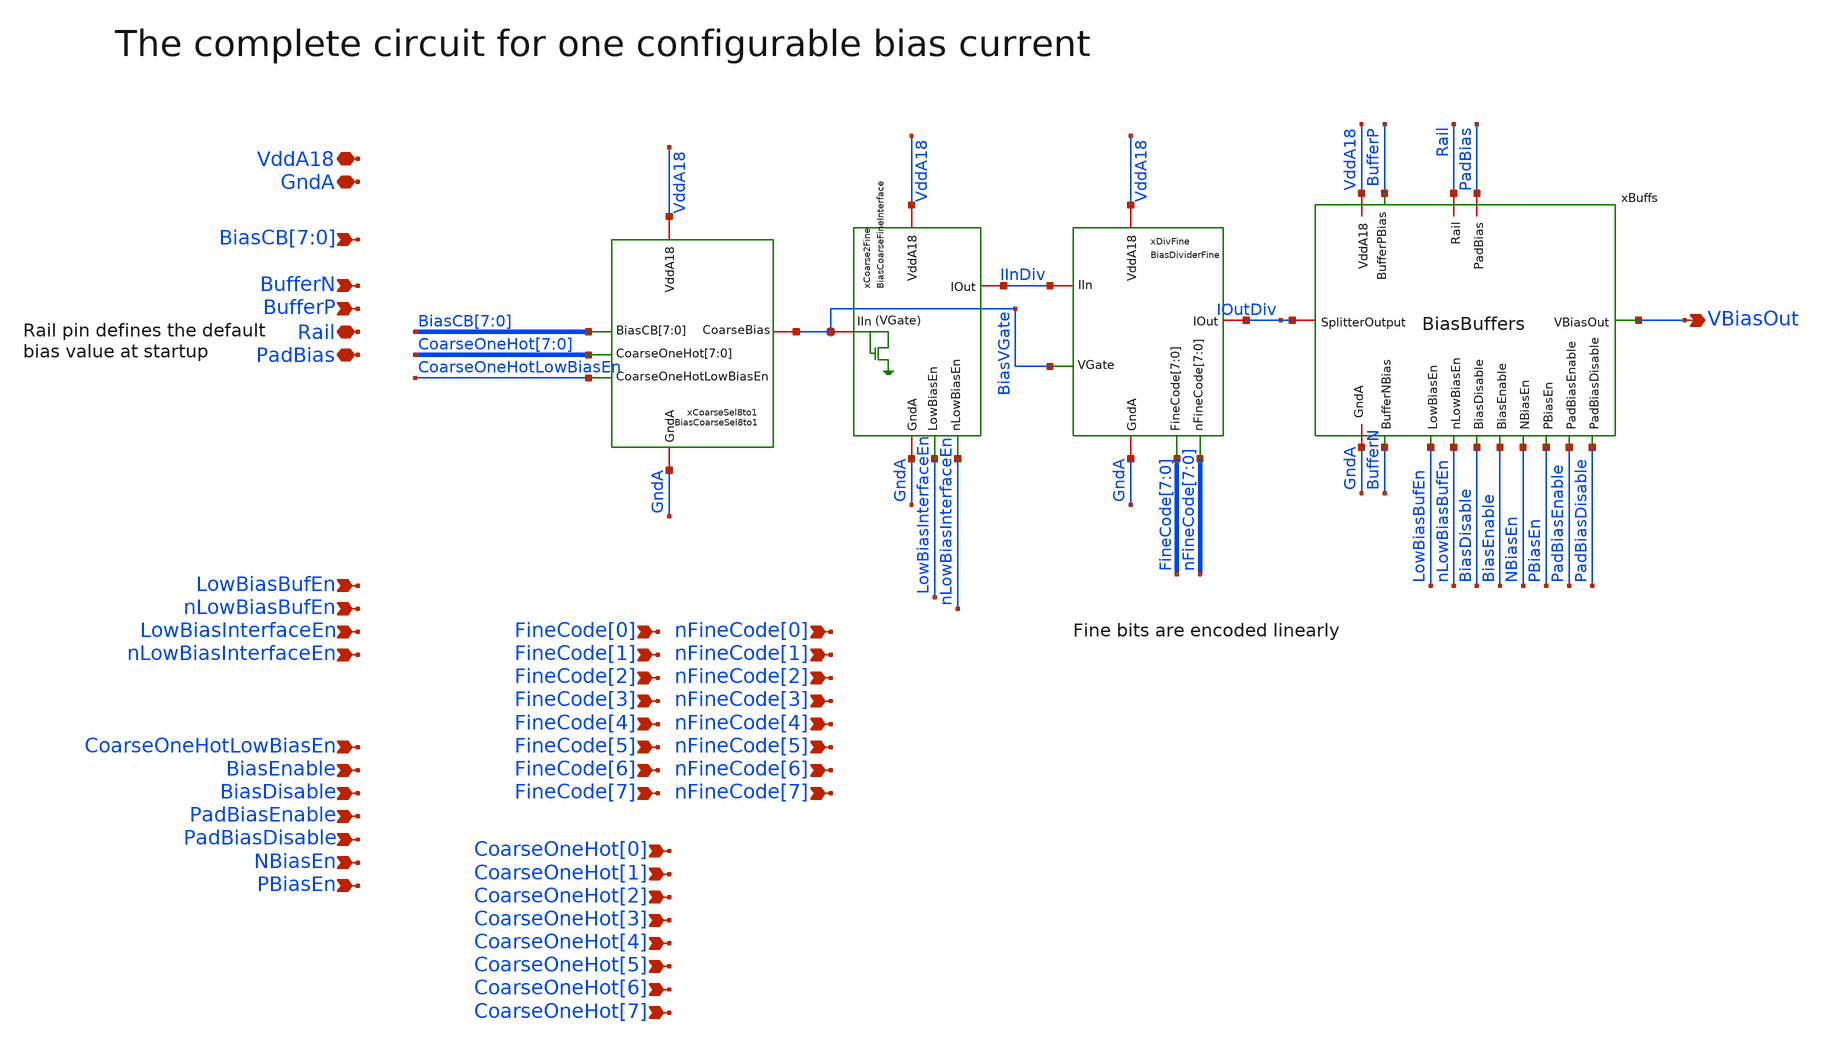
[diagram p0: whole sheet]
** sch_path: analog/xschem/BiasBranch.sch
**.subckt BiasBranch VddA18 GndA VBiasOut
*+ BiasCB[7],BiasCB[6],BiasCB[5],BiasCB[4],BiasCB[3],BiasCB[2],BiasCB[1],BiasCB[0] BufferN BufferP Rail LowBiasInterfaceEn nLowBiasInterfaceEn CoarseOneHotLowBiasEn LowBiasBufEn
*+ nLowBiasBufEn BiasEnable BiasDisable NBiasEn PBiasEn FineCode[0] FineCode[1] FineCode[2] FineCode[3] FineCode[4]
*+ FineCode[5] FineCode[6] FineCode[7] nFineCode[0] nFineCode[1] nFineCode[2] nFineCode[3] nFineCode[4]
*+ nFineCode[5] nFineCode[6] nFineCode[7] CoarseOneHot[0] CoarseOneHot[1] CoarseOneHot[2] CoarseOneHot[3]
*+ CoarseOneHot[4] CoarseOneHot[5] CoarseOneHot[6] CoarseOneHot[7] PadBiasEnable PadBiasDisable PadBias
*.iopin VddA18
*.iopin GndA
*.opin VBiasOut
*.ipin BiasCB[7],BiasCB[6],BiasCB[5],BiasCB[4],BiasCB[3],BiasCB[2],BiasCB[1],BiasCB[0]
*.ipin BufferN
*.ipin BufferP
*.iopin Rail
*.ipin LowBiasInterfaceEn
*.ipin nLowBiasInterfaceEn
*.ipin CoarseOneHotLowBiasEn
*.ipin LowBiasBufEn
*.ipin nLowBiasBufEn
*.ipin BiasEnable
*.ipin BiasDisable
*.ipin NBiasEn
*.ipin PBiasEn
*.ipin FineCode[0]
*.ipin FineCode[1]
*.ipin FineCode[2]
*.ipin FineCode[3]
*.ipin FineCode[4]
*.ipin FineCode[5]
*.ipin FineCode[6]
*.ipin FineCode[7]
*.ipin nFineCode[0]
*.ipin nFineCode[1]
*.ipin nFineCode[2]
*.ipin nFineCode[3]
*.ipin nFineCode[4]
*.ipin nFineCode[5]
*.ipin nFineCode[6]
*.ipin nFineCode[7]
*.ipin CoarseOneHot[0]
*.ipin CoarseOneHot[1]
*.ipin CoarseOneHot[2]
*.ipin CoarseOneHot[3]
*.ipin CoarseOneHot[4]
*.ipin CoarseOneHot[5]
*.ipin CoarseOneHot[6]
*.ipin CoarseOneHot[7]
*.ipin PadBiasEnable
*.ipin PadBiasDisable
*.iopin PadBias
xCoarse2Fine VddA18 GndA LowBiasInterfaceEn nLowBiasInterfaceEn BiasVGate IInDiv
+ BiasCoarseFineInterface
xDivFine VddA18 GndA FineCode[7] FineCode[6] FineCode[5] FineCode[4] FineCode[3] FineCode[2]
+ FineCode[1] FineCode[0] nFineCode[7] nFineCode[6] nFineCode[5] nFineCode[4] nFineCode[3] nFineCode[2]
+ nFineCode[1] nFineCode[0] IInDiv IOutDiv BiasVGate BiasDividerFine
xBuffs VddA18 GndA NBiasEn PBiasEn PadBiasDisable PadBiasEnable BiasDisable BiasEnable LowBiasBufEn
+ nLowBiasBufEn BufferN BufferP IOutDiv Rail VBiasOut PadBias BiasBuffers
xCoarseSel8to1 VddA18 GndA CoarseOneHot[7] CoarseOneHot[6] CoarseOneHot[5] CoarseOneHot[4]
+ CoarseOneHot[3] CoarseOneHot[2] CoarseOneHot[1] CoarseOneHot[0] CoarseOneHotLowBiasEn BiasCB[7] BiasCB[6] BiasCB[5]
+ BiasCB[4] BiasCB[3] BiasCB[2] BiasCB[1] BiasCB[0] BiasVGate BiasCoarseSel8to1
**.ends

* expanding   symbol:  BiasCoarseFineInterface.sym # of pins=6
** sym_path: analog/xschem/BiasCoarseFineInterface.sym
** sch_path: analog/xschem/BiasCoarseFineInterface.sch
.subckt BiasCoarseFineInterface VddA18 GndA LowBiasEn nLowBiasEn IIn IOut
*.iopin GndA
*.iopin VddA18
*.iopin IIn
*.iopin IOut
*.ipin nLowBiasEn
*.ipin LowBiasEn
XMpDisableHighBias HighBiasDioGate nLowBiasEn VddA18 VddA18 sky130_fd_pr__pfet_01v8 L=0.15 W=0.42 nf=1
+ ad='int((1 + 1)/2) * 0.42 / 1 * 0.29' as='int((1 + 2)/2) * 0.42 / 1 * 0.29' pd='2*int((1 + 1)/2) * (0.42 / 1 + 0.29)'
+ ps='2*int((1 + 2)/2) * (0.42 / 1 + 0.29)' nrd='0.29 / 0.42 ' nrs='0.29 / 0.42 ' sa=0 sb=0 sd=0 mult=1
+ m=1
XMpDioHighBias HighBiasDioDrain HighBiasDioGate VddA18 VddA18 sky130_fd_pr__pfet_01v8 L=1 W=32 nf=2 ad='int((2 + 1)/2) * 32 / 2 * 0.29'
+ as='int((2 + 2)/2) * 32 / 2 * 0.29' pd='2*int((2 + 1)/2) * (32 / 2 + 0.29)' ps='2*int((2 + 2)/2) * (32 / 2 + 0.29)'
+ nrd='0.29 / 32 ' nrs='0.29 / 32 ' sa=0 sb=0 sd=0 mult=8 m=8
XMpMirrHighBias HighBiasMirr HighBiasDioGate VddA18 VddA18 sky130_fd_pr__pfet_01v8 L=1 W=32 nf=2 ad='int((2 + 1)/2) * 32 / 2 * 0.29'
+ as='int((2 + 2)/2) * 32 / 2 * 0.29' pd='2*int((2 + 1)/2) * (32 / 2 + 0.29)' ps='2*int((2 + 2)/2) * (32 / 2 + 0.29)'
+ nrd='0.29 / 32 ' nrs='0.29 / 32 ' sa=0 sb=0 sd=0 mult=8 m=8
XMpswDioHighBias HighBiasDioGate LowBiasEn HighBiasDioDrain VddA18 sky130_fd_pr__pfet_01v8 L=0.5 W=0.42
+ nf=1 ad='int((1 + 1)/2) * 0.42 / 1 * 0.29' as='int((1 + 2)/2) * 0.42 / 1 * 0.29' pd='2*int((1 + 1)/2) * (0.42 / 1 + 0.29)'
+ ps='2*int((1 + 2)/2) * (0.42 / 1 + 0.29)' nrd='0.29 / 0.42 ' nrs='0.29 / 0.42 ' sa=0 sb=0 sd=0 mult=1
+ m=1
XMnDisableDioHighBias HighBiasDioDrain LowBiasEn GndA GndA sky130_fd_pr__nfet_01v8 L=0.15 W=0.42 nf=1
+ ad='int((1 + 1)/2) * 0.42 / 1 * 0.29' as='int((1 + 2)/2) * 0.42 / 1 * 0.29' pd='2*int((1 + 1)/2) * (0.42 / 1 + 0.29)'
+ ps='2*int((1 + 2)/2) * (0.42 / 1 + 0.29)' nrd='0.29 / 0.42 ' nrs='0.29 / 0.42 ' sa=0 sb=0 sd=0 mult=1
+ m=1
XMpSelDioHighBias net1 LowBiasEn HighBiasDioDrain VddA18 sky130_fd_pr__pfet_01v8_hvt L=0.5 W=32 nf=2
+ ad='int((2 + 1)/2) * 32 / 2 * 0.29' as='int((2 + 2)/2) * 32 / 2 * 0.29' pd='2*int((2 + 1)/2) * (32 / 2 + 0.29)'
+ ps='2*int((2 + 2)/2) * (32 / 2 + 0.29)' nrd='0.29 / 32 ' nrs='0.29 / 32 ' sa=0 sb=0 sd=0 mult=8 m=8
XMpSelMirrHighBias IOut LowBiasEn HighBiasMirr VddA18 sky130_fd_pr__pfet_01v8_hvt L=0.5 W=32 nf=2 ad='int((2 + 1)/2) * 32 / 2 * 0.29'
+ as='int((2 + 2)/2) * 32 / 2 * 0.29' pd='2*int((2 + 1)/2) * (32 / 2 + 0.29)' ps='2*int((2 + 2)/2) * (32 / 2 + 0.29)'
+ nrd='0.29 / 32 ' nrs='0.29 / 32 ' sa=0 sb=0 sd=0 mult=8 m=8
XMnDisableOutMirr HighBiasMirr LowBiasEn GndA GndA sky130_fd_pr__nfet_01v8 L=0.15 W=0.42 nf=1 ad='int((1 + 1)/2) * 0.42 / 1 * 0.29'
+ as='int((1 + 2)/2) * 0.42 / 1 * 0.29' pd='2*int((1 + 1)/2) * (0.42 / 1 + 0.29)' ps='2*int((1 + 2)/2) * (0.42 / 1 + 0.29)'
+ nrd='0.29 / 0.42 ' nrs='0.29 / 0.42 ' sa=0 sb=0 sd=0 mult=1 m=1
XMpInDio IIn IIn net1 VddA18 sky130_fd_pr__pfet_01v8_lvt L=1 W=9 nf=1 ad='int((1 + 1)/2) * 9 / 1 * 0.29'
+ as='int((1 + 2)/2) * 9 / 1 * 0.29' pd='2*int((1 + 1)/2) * (9 / 1 + 0.29)' ps='2*int((1 + 2)/2) * (9 / 1 + 0.29)'
+ nrd='0.29 / 9 ' nrs='0.29 / 9 ' sa=0 sb=0 sd=0 mult=2 m=2
XMpDioLowBias1 LowBiasDioInt LowBiasDioGate VddA18 VddA18 sky130_fd_pr__pfet_01v8 L=2 W=4 nf=1 ad='int((1 + 1)/2) * 4 / 1 * 0.29'
+ as='int((1 + 2)/2) * 4 / 1 * 0.29' pd='2*int((1 + 1)/2) * (4 / 1 + 0.29)' ps='2*int((1 + 2)/2) * (4 / 1 + 0.29)'
+ nrd='0.29 / 4 ' nrs='0.29 / 4 ' sa=0 sb=0 sd=0 mult=2 m=2
XMpMirrLowBias1 LowBiasMirrInt LowBiasDioGate VddA18 VddA18 sky130_fd_pr__pfet_01v8 L=2 W=4 nf=1 ad='int((1 + 1)/2) * 4 / 1 * 0.29'
+ as='int((1 + 2)/2) * 4 / 1 * 0.29' pd='2*int((1 + 1)/2) * (4 / 1 + 0.29)' ps='2*int((1 + 2)/2) * (4 / 1 + 0.29)'
+ nrd='0.29 / 4 ' nrs='0.29 / 4 ' sa=0 sb=0 sd=0 mult=2 m=2
XMpDioLowBias2 LowBiasDioGate LowBiasDioGate LowBiasDioInt VddA18 sky130_fd_pr__pfet_01v8 L=2 W=4 nf=1
+ ad='int((1 + 1)/2) * 4 / 1 * 0.29' as='int((1 + 2)/2) * 4 / 1 * 0.29' pd='2*int((1 + 1)/2) * (4 / 1 + 0.29)'
+ ps='2*int((1 + 2)/2) * (4 / 1 + 0.29)' nrd='0.29 / 4 ' nrs='0.29 / 4 ' sa=0 sb=0 sd=0 mult=2 m=2
XMpMirrLowBias2 LowBiasMirr LowBiasDioGate LowBiasMirrInt VddA18 sky130_fd_pr__pfet_01v8 L=2 W=4 nf=1
+ ad='int((1 + 1)/2) * 4 / 1 * 0.29' as='int((1 + 2)/2) * 4 / 1 * 0.29' pd='2*int((1 + 1)/2) * (4 / 1 + 0.29)'
+ ps='2*int((1 + 2)/2) * (4 / 1 + 0.29)' nrd='0.29 / 4 ' nrs='0.29 / 4 ' sa=0 sb=0 sd=0 mult=2 m=2
XMpSelDioLowBias net1 nLowBiasEn LowBiasDioGate VddA18 sky130_fd_pr__pfet_01v8_lvt L=2 W=4 nf=1 ad='int((1 + 1)/2) * 4 / 1 * 0.29'
+ as='int((1 + 2)/2) * 4 / 1 * 0.29' pd='2*int((1 + 1)/2) * (4 / 1 + 0.29)' ps='2*int((1 + 2)/2) * (4 / 1 + 0.29)'
+ nrd='0.29 / 4 ' nrs='0.29 / 4 ' sa=0 sb=0 sd=0 mult=2 m=2
XMpSelMirrLowBias IOut nLowBiasEn LowBiasMirr VddA18 sky130_fd_pr__pfet_01v8_lvt L=2 W=4 nf=1 ad='int((1 + 1)/2) * 4 / 1 * 0.29'
+ as='int((1 + 2)/2) * 4 / 1 * 0.29' pd='2*int((1 + 1)/2) * (4 / 1 + 0.29)' ps='2*int((1 + 2)/2) * (4 / 1 + 0.29)'
+ nrd='0.29 / 4 ' nrs='0.29 / 4 ' sa=0 sb=0 sd=0 mult=2 m=2
XMpDum1 net2 VddA18 VddA18 VddA18 sky130_fd_pr__pfet_01v8 L=0.5 W=16 nf=1 ad='int((1 + 1)/2) * 16 / 1 * 0.29'
+ as='int((1 + 2)/2) * 16 / 1 * 0.29' pd='2*int((1 + 1)/2) * (16 / 1 + 0.29)' ps='2*int((1 + 2)/2) * (16 / 1 + 0.29)'
+ nrd='0.29 / 16 ' nrs='0.29 / 16 ' sa=0 sb=0 sd=0 mult=1 m=1
XMpDum2 net3 VddA18 VddA18 VddA18 sky130_fd_pr__pfet_01v8 L=0.5 W=16 nf=1 ad='int((1 + 1)/2) * 16 / 1 * 0.29'
+ as='int((1 + 2)/2) * 16 / 1 * 0.29' pd='2*int((1 + 1)/2) * (16 / 1 + 0.29)' ps='2*int((1 + 2)/2) * (16 / 1 + 0.29)'
+ nrd='0.29 / 16 ' nrs='0.29 / 16 ' sa=0 sb=0 sd=0 mult=1 m=1
XMpDum3 net4 VddA18 VddA18 VddA18 sky130_fd_pr__pfet_01v8 L=0.2 W=4 nf=1 ad='int((1 + 1)/2) * 4 / 1 * 0.29'
+ as='int((1 + 2)/2) * 4 / 1 * 0.29' pd='2*int((1 + 1)/2) * (4 / 1 + 0.29)' ps='2*int((1 + 2)/2) * (4 / 1 + 0.29)'
+ nrd='0.29 / 4 ' nrs='0.29 / 4 ' sa=0 sb=0 sd=0 mult=1 m=1
XMpDum4 net5 VddA18 VddA18 VddA18 sky130_fd_pr__pfet_01v8 L=0.2 W=4 nf=1 ad='int((1 + 1)/2) * 4 / 1 * 0.29'
+ as='int((1 + 2)/2) * 4 / 1 * 0.29' pd='2*int((1 + 1)/2) * (4 / 1 + 0.29)' ps='2*int((1 + 2)/2) * (4 / 1 + 0.29)'
+ nrd='0.29 / 4 ' nrs='0.29 / 4 ' sa=0 sb=0 sd=0 mult=1 m=1
XMpDum5 net6 VddA18 VddA18 VddA18 sky130_fd_pr__pfet_01v8 L=0.2 W=4 nf=1 ad='int((1 + 1)/2) * 4 / 1 * 0.29'
+ as='int((1 + 2)/2) * 4 / 1 * 0.29' pd='2*int((1 + 1)/2) * (4 / 1 + 0.29)' ps='2*int((1 + 2)/2) * (4 / 1 + 0.29)'
+ nrd='0.29 / 4 ' nrs='0.29 / 4 ' sa=0 sb=0 sd=0 mult=1 m=1
XMpDum6 net7 VddA18 VddA18 VddA18 sky130_fd_pr__pfet_01v8 L=0.2 W=4 nf=1 ad='int((1 + 1)/2) * 4 / 1 * 0.29'
+ as='int((1 + 2)/2) * 4 / 1 * 0.29' pd='2*int((1 + 1)/2) * (4 / 1 + 0.29)' ps='2*int((1 + 2)/2) * (4 / 1 + 0.29)'
+ nrd='0.29 / 4 ' nrs='0.29 / 4 ' sa=0 sb=0 sd=0 mult=1 m=1
XMpDum7 net8 VddA18 VddA18 VddA18 sky130_fd_pr__pfet_01v8 L=0.2 W=4 nf=1 ad='int((1 + 1)/2) * 4 / 1 * 0.29'
+ as='int((1 + 2)/2) * 4 / 1 * 0.29' pd='2*int((1 + 1)/2) * (4 / 1 + 0.29)' ps='2*int((1 + 2)/2) * (4 / 1 + 0.29)'
+ nrd='0.29 / 4 ' nrs='0.29 / 4 ' sa=0 sb=0 sd=0 mult=1 m=1
* noconn #net2
* noconn #net3
* noconn #net4
* noconn #net5
* noconn #net6
* noconn #net7
* noconn #net8
.ends


* expanding   symbol:  BiasDividerFine.sym # of pins=7
** sym_path: analog/klayout/production/final_merge_20260923/testbenches/cace/analog/xschem/BiasDividerFine.sym
** sch_path: analog/klayout/production/final_merge_20260923/testbenches/cace/analog/xschem/BiasDividerFine.sch
.subckt BiasDividerFine VddA18 GndA FineCode[7] FineCode[6] FineCode[5] FineCode[4] FineCode[3]
+ FineCode[2] FineCode[1] FineCode[0] nFineCode[7] nFineCode[6] nFineCode[5] nFineCode[4] nFineCode[3]
+ nFineCode[2] nFineCode[1] nFineCode[0] IIn IOut VGate
*.iopin VddA18
*.iopin GndA
*.iopin IOut
*.ipin
*+ FineCode[7],FineCode[6],FineCode[5],FineCode[4],FineCode[3],FineCode[2],FineCode[1],FineCode[0]
*.ipin VGate
*.iopin IIn
*.ipin
*+ nFineCode[7],nFineCode[6],nFineCode[5],nFineCode[4],nFineCode[3],nFineCode[2],nFineCode[1],nFineCode[0]
xdiv0 Idiv1 Idiv0 VGate IOut VddA18 termDio nFineCode[0] FineCode[0] BiasDividerFineCell
xdiv1 Idiv2 Idiv1 VGate IOut VddA18 termDio nFineCode[1] FineCode[1] BiasDividerFineCell
xdiv2 Idiv3 Idiv2 VGate IOut VddA18 termDio nFineCode[2] FineCode[2] BiasDividerFineCell
xdiv3 Idiv4 Idiv3 VGate IOut VddA18 termDio nFineCode[3] FineCode[3] BiasDividerFineCell
xdiv4 Idiv5 Idiv4 VGate IOut VddA18 termDio nFineCode[4] FineCode[4] BiasDividerFineCell
xdiv5 Idiv6 Idiv5 VGate IOut VddA18 termDio nFineCode[5] FineCode[5] BiasDividerFineCell
xdiv6 Idiv7 Idiv6 VGate IOut VddA18 termDio nFineCode[6] FineCode[6] BiasDividerFineCell
xdiv7 IIn Idiv7 VGate IOut VddA18 termDio nFineCode[7] FineCode[7] BiasDividerFineCell
XMrTerm termDio VGate Idiv0 VddA18 sky130_fd_pr__pfet_01v8_lvt L=1 W=9 nf=1 ad='int((1 + 1)/2) * 9 / 1 * 0.29'
+ as='int((1 + 2)/2) * 9 / 1 * 0.29' pd='2*int((1 + 1)/2) * (9 / 1 + 0.29)' ps='2*int((1 + 2)/2) * (9 / 1 + 0.29)'
+ nrd='0.29 / 9 ' nrs='0.29 / 9 ' sa=0 sb=0 sd=0 mult=2 m=2
XMnterm termDio termDio GndA GndA sky130_fd_pr__nfet_01v8_lvt L=0.8 W=8 nf=1 ad='int((1 + 1)/2) * 8 / 1 * 0.29'
+ as='int((1 + 2)/2) * 8 / 1 * 0.29' pd='2*int((1 + 1)/2) * (8 / 1 + 0.29)' ps='2*int((1 + 2)/2) * (8 / 1 + 0.29)'
+ nrd='0.29 / 8 ' nrs='0.29 / 8 ' sa=0 sb=0 sd=0 mult=1 m=1
.ends


* expanding   symbol:  BiasBuffers.sym # of pins=16
** sym_path: analog/xschem/BiasBuffers.sym
** sch_path: analog/xschem/BiasBuffers.sch
.subckt BiasBuffers VddA18 GndA NBiasEn PBiasEn PadBiasDisable PadBiasEnable BiasDisable BiasEnable
+ LowBiasEn nLowBiasEn BufferNBias BufferPBias SplitterOutput Rail VBiasOut PadBias
*.iopin GndA
*.iopin VddA18
*.opin VBiasOut
*.ipin NBiasEn
*.ipin PBiasEn
*.ipin BiasDisable
*.ipin BiasEnable
*.ipin LowBiasEn
*.ipin BufferNBias
*.ipin BufferPBias
*.iopin SplitterOutput
*.iopin Rail
*.ipin nLowBiasEn
*.ipin PadBiasDisable
*.ipin PadBiasEnable
*.iopin PadBias
XMnDio SplitterOutput NBias GndA GndA sky130_fd_pr__nfet_01v8 L=6 W=6 nf=1 ad='int((1 + 1)/2) * 6 / 1 * 0.29'
+ as='int((1 + 2)/2) * 6 / 1 * 0.29' pd='2*int((1 + 1)/2) * (6 / 1 + 0.29)' ps='2*int((1 + 2)/2) * (6 / 1 + 0.29)'
+ nrd='0.29 / 6 ' nrs='0.29 / 6 ' sa=0 sb=0 sd=0 mult=1 m=1
XMnswnMirrnB0 net1 LowBiasEn NBias GndA sky130_fd_pr__nfet_01v8 L=0.15 W=1 nf=1 ad='int((1 + 1)/2) * 1 / 1 * 0.29'
+ as='int((1 + 2)/2) * 1 / 1 * 0.29' pd='2*int((1 + 1)/2) * (1 / 1 + 0.29)' ps='2*int((1 + 2)/2) * (1 / 1 + 0.29)'
+ nrd='0.29 / 1 ' nrs='0.29 / 1 ' sa=0 sb=0 sd=0 mult=1 m=1
XMpswnMirrnB0 NBias nLowBiasEn net1 VddA18 sky130_fd_pr__pfet_01v8 L=0.38 W=1 nf=1 ad='int((1 + 1)/2) * 1 / 1 * 0.29'
+ as='int((1 + 2)/2) * 1 / 1 * 0.29' pd='2*int((1 + 1)/2) * (1 / 1 + 0.29)' ps='2*int((1 + 2)/2) * (1 / 1 + 0.29)'
+ nrd='0.29 / 1 ' nrs='0.29 / 1 ' sa=0 sb=0 sd=0 mult=1 m=1
XMnMirrBuffB0 nMirrBuffDrain SplitterOutput net2 GndA sky130_fd_pr__nfet_01v8_lvt L=2.4 W=0.5 nf=1 ad='int((1 + 1)/2) * 0.5 / 1 * 0.29'
+ as='int((1 + 2)/2) * 0.5 / 1 * 0.29' pd='2*int((1 + 1)/2) * (0.5 / 1 + 0.29)' ps='2*int((1 + 2)/2) * (0.5 / 1 + 0.29)'
+ nrd='0.29 / 0.5 ' nrs='0.29 / 0.5 ' sa=0 sb=0 sd=0 mult=1 m=1
XMpnMirrEnable nMirrBuffDrain BiasDisable VddA18 VddA18 sky130_fd_pr__pfet_01v8 L=0.15 W=1 nf=1 ad='int((1 + 1)/2) * 1 / 1 * 0.29'
+ as='int((1 + 2)/2) * 1 / 1 * 0.29' pd='2*int((1 + 1)/2) * (1 / 1 + 0.29)' ps='2*int((1 + 2)/2) * (1 / 1 + 0.29)'
+ nrd='0.29 / 1 ' nrs='0.29 / 1 ' sa=0 sb=0 sd=0 mult=1 m=1
XMnswnMirrB0 net2 nLowBiasEn NBias GndA sky130_fd_pr__nfet_01v8 L=0.15 W=1 nf=1 ad='int((1 + 1)/2) * 1 / 1 * 0.29'
+ as='int((1 + 2)/2) * 1 / 1 * 0.29' pd='2*int((1 + 1)/2) * (1 / 1 + 0.29)' ps='2*int((1 + 2)/2) * (1 / 1 + 0.29)'
+ nrd='0.29 / 1 ' nrs='0.29 / 1 ' sa=0 sb=0 sd=0 mult=1 m=1
XMpswnMirrB0 NBias LowBiasEn net2 VddA18 sky130_fd_pr__pfet_01v8 L=0.38 W=1 nf=1 ad='int((1 + 1)/2) * 1 / 1 * 0.29'
+ as='int((1 + 2)/2) * 1 / 1 * 0.29' pd='2*int((1 + 1)/2) * (1 / 1 + 0.29)' ps='2*int((1 + 2)/2) * (1 / 1 + 0.29)'
+ nrd='0.29 / 1 ' nrs='0.29 / 1 ' sa=0 sb=0 sd=0 mult=1 m=1
XMnMirr nCopy NBias GndA GndA sky130_fd_pr__nfet_01v8 L=6 W=6 nf=1 ad='int((1 + 1)/2) * 6 / 1 * 0.29'
+ as='int((1 + 2)/2) * 6 / 1 * 0.29' pd='2*int((1 + 1)/2) * (6 / 1 + 0.29)' ps='2*int((1 + 2)/2) * (6 / 1 + 0.29)'
+ nrd='0.29 / 6 ' nrs='0.29 / 6 ' sa=0 sb=0 sd=0 mult=1 m=1
XMnMirrBuffBias NBias BufferNBias GndA GndA sky130_fd_pr__nfet_01v8_lvt L=6 W=6 nf=1 ad='int((1 + 1)/2) * 6 / 1 * 0.29'
+ as='int((1 + 2)/2) * 6 / 1 * 0.29' pd='2*int((1 + 1)/2) * (6 / 1 + 0.29)' ps='2*int((1 + 2)/2) * (6 / 1 + 0.29)'
+ nrd='0.29 / 6 ' nrs='0.29 / 6 ' sa=0 sb=0 sd=0 mult=16 m=16
XMpDio nCopy PBias VddA18 VddA18 sky130_fd_pr__pfet_01v8 L=3 W=6 nf=1 ad='int((1 + 1)/2) * 6 / 1 * 0.29'
+ as='int((1 + 2)/2) * 6 / 1 * 0.29' pd='2*int((1 + 1)/2) * (6 / 1 + 0.29)' ps='2*int((1 + 2)/2) * (6 / 1 + 0.29)'
+ nrd='0.29 / 6 ' nrs='0.29 / 6 ' sa=0 sb=0 sd=0 mult=2 m=2
XMnswpMirrnB0 PBias LowBiasEn net3 GndA sky130_fd_pr__nfet_01v8 L=0.15 W=1 nf=1 ad='int((1 + 1)/2) * 1 / 1 * 0.29'
+ as='int((1 + 2)/2) * 1 / 1 * 0.29' pd='2*int((1 + 1)/2) * (1 / 1 + 0.29)' ps='2*int((1 + 2)/2) * (1 / 1 + 0.29)'
+ nrd='0.29 / 1 ' nrs='0.29 / 1 ' sa=0 sb=0 sd=0 mult=1 m=1
XMpswpMirrnB0 net3 nLowBiasEn PBias VddA18 sky130_fd_pr__pfet_01v8 L=0.38 W=1 nf=1 ad='int((1 + 1)/2) * 1 / 1 * 0.29'
+ as='int((1 + 2)/2) * 1 / 1 * 0.29' pd='2*int((1 + 1)/2) * (1 / 1 + 0.29)' ps='2*int((1 + 2)/2) * (1 / 1 + 0.29)'
+ nrd='0.29 / 1 ' nrs='0.29 / 1 ' sa=0 sb=0 sd=0 mult=1 m=1
XMnswpMirrB0 PBias nLowBiasEn net4 GndA sky130_fd_pr__nfet_01v8 L=0.15 W=1 nf=1 ad='int((1 + 1)/2) * 1 / 1 * 0.29'
+ as='int((1 + 2)/2) * 1 / 1 * 0.29' pd='2*int((1 + 1)/2) * (1 / 1 + 0.29)' ps='2*int((1 + 2)/2) * (1 / 1 + 0.29)'
+ nrd='0.29 / 1 ' nrs='0.29 / 1 ' sa=0 sb=0 sd=0 mult=1 m=1
XMpswpMirrB0 net4 LowBiasEn PBias VddA18 sky130_fd_pr__pfet_01v8 L=0.38 W=1 nf=1 ad='int((1 + 1)/2) * 1 / 1 * 0.29'
+ as='int((1 + 2)/2) * 1 / 1 * 0.29' pd='2*int((1 + 1)/2) * (1 / 1 + 0.29)' ps='2*int((1 + 2)/2) * (1 / 1 + 0.29)'
+ nrd='0.29 / 1 ' nrs='0.29 / 1 ' sa=0 sb=0 sd=0 mult=1 m=1
XMpMirrBuffnB0 net3 nCopy pMirrBuffDrain VddA18 sky130_fd_pr__pfet_01v8_lvt L=0.38 W=2.4 nf=1 ad='int((1 + 1)/2) * 2.4 / 1 * 0.29'
+ as='int((1 + 2)/2) * 2.4 / 1 * 0.29' pd='2*int((1 + 1)/2) * (2.4 / 1 + 0.29)' ps='2*int((1 + 2)/2) * (2.4 / 1 + 0.29)'
+ nrd='0.29 / 2.4 ' nrs='0.29 / 2.4 ' sa=0 sb=0 sd=0 mult=6 m=6
XMpMirrBuffB0 net4 nCopy pMirrBuffDrain VddA18 sky130_fd_pr__pfet_01v8_lvt L=2.4 W=0.5 nf=1 ad='int((1 + 1)/2) * 0.5 / 1 * 0.29'
+ as='int((1 + 2)/2) * 0.5 / 1 * 0.29' pd='2*int((1 + 1)/2) * (0.5 / 1 + 0.29)' ps='2*int((1 + 2)/2) * (0.5 / 1 + 0.29)'
+ nrd='0.29 / 0.5 ' nrs='0.29 / 0.5 ' sa=0 sb=0 sd=0 mult=1 m=1
XMnpMirrEnable pMirrBuffDrain PBiasEn GndA GndA sky130_fd_pr__nfet_01v8 L=0.15 W=1 nf=1 ad='int((1 + 1)/2) * 1 / 1 * 0.29'
+ as='int((1 + 2)/2) * 1 / 1 * 0.29' pd='2*int((1 + 1)/2) * (1 / 1 + 0.29)' ps='2*int((1 + 2)/2) * (1 / 1 + 0.29)'
+ nrd='0.29 / 1 ' nrs='0.29 / 1 ' sa=0 sb=0 sd=0 mult=1 m=1
XMpMirrBuffBias PBias BufferPBias VddA18 VddA18 sky130_fd_pr__pfet_01v8_lvt L=3 W=6 nf=1 ad='int((1 + 1)/2) * 6 / 1 * 0.29'
+ as='int((1 + 2)/2) * 6 / 1 * 0.29' pd='2*int((1 + 1)/2) * (6 / 1 + 0.29)' ps='2*int((1 + 2)/2) * (6 / 1 + 0.29)'
+ nrd='0.29 / 6 ' nrs='0.29 / 6 ' sa=0 sb=0 sd=0 mult=2 m=2
XMnswNBias NBias NBiasEn net5 GndA sky130_fd_pr__nfet_01v8 L=0.15 W=4 nf=1 ad='int((1 + 1)/2) * 4 / 1 * 0.29'
+ as='int((1 + 2)/2) * 4 / 1 * 0.29' pd='2*int((1 + 1)/2) * (4 / 1 + 0.29)' ps='2*int((1 + 2)/2) * (4 / 1 + 0.29)'
+ nrd='0.29 / 4 ' nrs='0.29 / 4 ' sa=0 sb=0 sd=0 mult=1 m=1
XMpswNBias net5 PBiasEn NBias VddA18 sky130_fd_pr__pfet_01v8 L=0.38 W=4 nf=1 ad='int((1 + 1)/2) * 4 / 1 * 0.29'
+ as='int((1 + 2)/2) * 4 / 1 * 0.29' pd='2*int((1 + 1)/2) * (4 / 1 + 0.29)' ps='2*int((1 + 2)/2) * (4 / 1 + 0.29)'
+ nrd='0.29 / 4 ' nrs='0.29 / 4 ' sa=0 sb=0 sd=0 mult=1 m=1
XMnswPBias net5 PBiasEn PBias GndA sky130_fd_pr__nfet_01v8 L=0.15 W=4 nf=1 ad='int((1 + 1)/2) * 4 / 1 * 0.29'
+ as='int((1 + 2)/2) * 4 / 1 * 0.29' pd='2*int((1 + 1)/2) * (4 / 1 + 0.29)' ps='2*int((1 + 2)/2) * (4 / 1 + 0.29)'
+ nrd='0.29 / 4 ' nrs='0.29 / 4 ' sa=0 sb=0 sd=0 mult=1 m=1
XMpswPBias PBias NBiasEn net5 VddA18 sky130_fd_pr__pfet_01v8 L=0.38 W=4 nf=1 ad='int((1 + 1)/2) * 4 / 1 * 0.29'
+ as='int((1 + 2)/2) * 4 / 1 * 0.29' pd='2*int((1 + 1)/2) * (4 / 1 + 0.29)' ps='2*int((1 + 2)/2) * (4 / 1 + 0.29)'
+ nrd='0.29 / 4 ' nrs='0.29 / 4 ' sa=0 sb=0 sd=0 mult=1 m=1
XMnswBias net6 BiasEnable VBiasOut GndA sky130_fd_pr__nfet_01v8 L=0.15 W=4 nf=1 ad='int((1 + 1)/2) * 4 / 1 * 0.29'
+ as='int((1 + 2)/2) * 4 / 1 * 0.29' pd='2*int((1 + 1)/2) * (4 / 1 + 0.29)' ps='2*int((1 + 2)/2) * (4 / 1 + 0.29)'
+ nrd='0.29 / 4 ' nrs='0.29 / 4 ' sa=0 sb=0 sd=0 mult=1 m=1
XMpswBias VBiasOut BiasDisable net6 VddA18 sky130_fd_pr__pfet_01v8 L=0.38 W=4 nf=1 ad='int((1 + 1)/2) * 4 / 1 * 0.29'
+ as='int((1 + 2)/2) * 4 / 1 * 0.29' pd='2*int((1 + 1)/2) * (4 / 1 + 0.29)' ps='2*int((1 + 2)/2) * (4 / 1 + 0.29)'
+ nrd='0.29 / 4 ' nrs='0.29 / 4 ' sa=0 sb=0 sd=0 mult=1 m=1
XMnswRail VBiasOut BiasDisable Rail GndA sky130_fd_pr__nfet_01v8 L=0.15 W=4 nf=1 ad='int((1 + 1)/2) * 4 / 1 * 0.29'
+ as='int((1 + 2)/2) * 4 / 1 * 0.29' pd='2*int((1 + 1)/2) * (4 / 1 + 0.29)' ps='2*int((1 + 2)/2) * (4 / 1 + 0.29)'
+ nrd='0.29 / 4 ' nrs='0.29 / 4 ' sa=0 sb=0 sd=0 mult=1 m=1
XMpswRail Rail BiasEnable VBiasOut VddA18 sky130_fd_pr__pfet_01v8 L=0.38 W=4 nf=1 ad='int((1 + 1)/2) * 4 / 1 * 0.29'
+ as='int((1 + 2)/2) * 4 / 1 * 0.29' pd='2*int((1 + 1)/2) * (4 / 1 + 0.29)' ps='2*int((1 + 2)/2) * (4 / 1 + 0.29)'
+ nrd='0.29 / 4 ' nrs='0.29 / 4 ' sa=0 sb=0 sd=0 mult=1 m=1
XMnMirrBuffnB0 nMirrBuffDrain SplitterOutput net1 GndA sky130_fd_pr__nfet_01v8_lvt L=0.24 W=2.4 nf=1
+ ad='int((1 + 1)/2) * 2.4 / 1 * 0.29' as='int((1 + 2)/2) * 2.4 / 1 * 0.29' pd='2*int((1 + 1)/2) * (2.4 / 1 + 0.29)'
+ ps='2*int((1 + 2)/2) * (2.4 / 1 + 0.29)' nrd='0.29 / 2.4 ' nrs='0.29 / 2.4 ' sa=0 sb=0 sd=0 mult=10 m=10
XMnswBias1 net5 PadBiasDisable net6 GndA sky130_fd_pr__nfet_01v8 L=0.15 W=4 nf=1 ad='int((1 + 1)/2) * 4 / 1 * 0.29'
+ as='int((1 + 2)/2) * 4 / 1 * 0.29' pd='2*int((1 + 1)/2) * (4 / 1 + 0.29)' ps='2*int((1 + 2)/2) * (4 / 1 + 0.29)'
+ nrd='0.29 / 4 ' nrs='0.29 / 4 ' sa=0 sb=0 sd=0 mult=1 m=1
XMpswBias1 net6 PadBiasEnable net5 VddA18 sky130_fd_pr__pfet_01v8 L=0.38 W=4 nf=1 ad='int((1 + 1)/2) * 4 / 1 * 0.29'
+ as='int((1 + 2)/2) * 4 / 1 * 0.29' pd='2*int((1 + 1)/2) * (4 / 1 + 0.29)' ps='2*int((1 + 2)/2) * (4 / 1 + 0.29)'
+ nrd='0.29 / 4 ' nrs='0.29 / 4 ' sa=0 sb=0 sd=0 mult=1 m=1
XMnswRail1 net6 PadBiasEnable PadBias GndA sky130_fd_pr__nfet_01v8 L=0.15 W=4 nf=1 ad='int((1 + 1)/2) * 4 / 1 * 0.29'
+ as='int((1 + 2)/2) * 4 / 1 * 0.29' pd='2*int((1 + 1)/2) * (4 / 1 + 0.29)' ps='2*int((1 + 2)/2) * (4 / 1 + 0.29)'
+ nrd='0.29 / 4 ' nrs='0.29 / 4 ' sa=0 sb=0 sd=0 mult=1 m=1
XMpswRail1 PadBias PadBiasDisable net6 VddA18 sky130_fd_pr__pfet_01v8 L=0.38 W=4 nf=1 ad='int((1 + 1)/2) * 4 / 1 * 0.29'
+ as='int((1 + 2)/2) * 4 / 1 * 0.29' pd='2*int((1 + 1)/2) * (4 / 1 + 0.29)' ps='2*int((1 + 2)/2) * (4 / 1 + 0.29)'
+ nrd='0.29 / 4 ' nrs='0.29 / 4 ' sa=0 sb=0 sd=0 mult=1 m=1
.ends


* expanding   symbol:  BiasCoarseSel8to1.sym # of pins=6
** sym_path: analog/xschem/BiasCoarseSel8to1.sym
** sch_path: analog/xschem/BiasCoarseSel8to1.sch
.subckt BiasCoarseSel8to1 VddA18 GndA CoarseOneHot[7] CoarseOneHot[6] CoarseOneHot[5]
+ CoarseOneHot[4] CoarseOneHot[3] CoarseOneHot[2] CoarseOneHot[1] CoarseOneHot[0] CoarseOneHotLowBiasEn BiasCB[7]
+ BiasCB[6] BiasCB[5] BiasCB[4] BiasCB[3] BiasCB[2] BiasCB[1] BiasCB[0] CoarseBias
*.ipin BiasCB[7],BiasCB[6],BiasCB[5],BiasCB[4],BiasCB[3],BiasCB[2],BiasCB[1],BiasCB[0]
*.ipin
*+ CoarseOneHot[7],CoarseOneHot[6],CoarseOneHot[5],CoarseOneHot[4],CoarseOneHot[3],CoarseOneHot[2],CoarseOneHot[1],CoarseOneHot[0]
*.iopin CoarseBias
*.iopin VddA18
*.iopin GndA
*.ipin CoarseOneHotLowBiasEn
XMpswB0 net1 CoarseOneHot[0] VddA18 VddA18 sky130_fd_pr__pfet_01v8 L=0.15 W=0.55 nf=1 ad='int((1 + 1)/2) * 0.55 / 1 * 0.29'
+ as='int((1 + 2)/2) * 0.55 / 1 * 0.29' pd='2*int((1 + 1)/2) * (0.55 / 1 + 0.29)' ps='2*int((1 + 2)/2) * (0.55 / 1 + 0.29)'
+ nrd='0.29 / 0.55 ' nrs='0.29 / 0.55 ' sa=0 sb=0 sd=0 mult=1 m=1
XMnswuB0 CoarseBias CoarseOneHot[0] net1 GndA sky130_fd_pr__nfet_01v8 L=0.15 W=1 nf=1 ad='int((1 + 1)/2) * 1 / 1 * 0.29'
+ as='int((1 + 2)/2) * 1 / 1 * 0.29' pd='2*int((1 + 1)/2) * (1 / 1 + 0.29)' ps='2*int((1 + 2)/2) * (1 / 1 + 0.29)'
+ nrd='0.29 / 1 ' nrs='0.29 / 1 ' sa=0 sb=0 sd=0 mult=1 m=1
XMnswlB0 net1 CoarseOneHot[0] MirrB0_drain GndA sky130_fd_pr__nfet_01v8_lvt L=0.15 W=1 nf=1 ad='int((1 + 1)/2) * 1 / 1 * 0.29'
+ as='int((1 + 2)/2) * 1 / 1 * 0.29' pd='2*int((1 + 1)/2) * (1 / 1 + 0.29)' ps='2*int((1 + 2)/2) * (1 / 1 + 0.29)'
+ nrd='0.29 / 1 ' nrs='0.29 / 1 ' sa=0 sb=0 sd=0 mult=1 m=1
XMmirrB0 MirrB0_drain BiasCB[0] GndA GndA sky130_fd_pr__nfet_01v8_lvt L=5 W=1.8 nf=1 ad='int((1 + 1)/2) * 1.8 / 1 * 0.29'
+ as='int((1 + 2)/2) * 1.8 / 1 * 0.29' pd='2*int((1 + 1)/2) * (1.8 / 1 + 0.29)' ps='2*int((1 + 2)/2) * (1.8 / 1 + 0.29)'
+ nrd='0.29 / 1.8 ' nrs='0.29 / 1.8 ' sa=0 sb=0 sd=0 mult=8 m=8
XMpswB1 net2 CoarseOneHot[1] VddA18 VddA18 sky130_fd_pr__pfet_01v8 L=0.15 W=0.55 nf=1 ad='int((1 + 1)/2) * 0.55 / 1 * 0.29'
+ as='int((1 + 2)/2) * 0.55 / 1 * 0.29' pd='2*int((1 + 1)/2) * (0.55 / 1 + 0.29)' ps='2*int((1 + 2)/2) * (0.55 / 1 + 0.29)'
+ nrd='0.29 / 0.55 ' nrs='0.29 / 0.55 ' sa=0 sb=0 sd=0 mult=1 m=1
XMnswuB1 CoarseBias CoarseOneHot[1] net2 GndA sky130_fd_pr__nfet_01v8 L=1 W=1 nf=1 ad='int((1 + 1)/2) * 1 / 1 * 0.29'
+ as='int((1 + 2)/2) * 1 / 1 * 0.29' pd='2*int((1 + 1)/2) * (1 / 1 + 0.29)' ps='2*int((1 + 2)/2) * (1 / 1 + 0.29)'
+ nrd='0.29 / 1 ' nrs='0.29 / 1 ' sa=0 sb=0 sd=0 mult=1 m=1
XMnswlB1 net2 CoarseOneHot[1] MirrB1_drain GndA sky130_fd_pr__nfet_01v8 L=1 W=1 nf=1 ad='int((1 + 1)/2) * 1 / 1 * 0.29'
+ as='int((1 + 2)/2) * 1 / 1 * 0.29' pd='2*int((1 + 1)/2) * (1 / 1 + 0.29)' ps='2*int((1 + 2)/2) * (1 / 1 + 0.29)'
+ nrd='0.29 / 1 ' nrs='0.29 / 1 ' sa=0 sb=0 sd=0 mult=1 m=1
XMmirrB1 MirrB1_drain BiasCB[1] GndA GndA sky130_fd_pr__nfet_01v8_lvt L=9.98 W=0.98 nf=1 ad='int((1 + 1)/2) * 0.98 / 1 * 0.29'
+ as='int((1 + 2)/2) * 0.98 / 1 * 0.29' pd='2*int((1 + 1)/2) * (0.98 / 1 + 0.29)' ps='2*int((1 + 2)/2) * (0.98 / 1 + 0.29)'
+ nrd='0.29 / 0.98 ' nrs='0.29 / 0.98 ' sa=0 sb=0 sd=0 mult=8 m=8
XMpswB2 net3 CoarseOneHot[2] VddA18 VddA18 sky130_fd_pr__pfet_01v8 L=0.15 W=0.55 nf=1 ad='int((1 + 1)/2) * 0.55 / 1 * 0.29'
+ as='int((1 + 2)/2) * 0.55 / 1 * 0.29' pd='2*int((1 + 1)/2) * (0.55 / 1 + 0.29)' ps='2*int((1 + 2)/2) * (0.55 / 1 + 0.29)'
+ nrd='0.29 / 0.55 ' nrs='0.29 / 0.55 ' sa=0 sb=0 sd=0 mult=1 m=1
XMnswuB2 CoarseBias CoarseOneHot[2] net3 GndA sky130_fd_pr__nfet_01v8 L=1 W=1 nf=1 ad='int((1 + 1)/2) * 1 / 1 * 0.29'
+ as='int((1 + 2)/2) * 1 / 1 * 0.29' pd='2*int((1 + 1)/2) * (1 / 1 + 0.29)' ps='2*int((1 + 2)/2) * (1 / 1 + 0.29)'
+ nrd='0.29 / 1 ' nrs='0.29 / 1 ' sa=0 sb=0 sd=0 mult=1 m=1
XMnswlB2 net3 CoarseOneHot[2] MirrB2_drain GndA sky130_fd_pr__nfet_01v8 L=1 W=1 nf=1 ad='int((1 + 1)/2) * 1 / 1 * 0.29'
+ as='int((1 + 2)/2) * 1 / 1 * 0.29' pd='2*int((1 + 1)/2) * (1 / 1 + 0.29)' ps='2*int((1 + 2)/2) * (1 / 1 + 0.29)'
+ nrd='0.29 / 1 ' nrs='0.29 / 1 ' sa=0 sb=0 sd=0 mult=1 m=1
XMmirrhB2 MirrB2_drain BiasCB[2] net4 GndA sky130_fd_pr__nfet_01v8_lvt L=5 W=1.98 nf=1 ad='int((1 + 1)/2) * 1.98 / 1 * 0.29'
+ as='int((1 + 2)/2) * 1.98 / 1 * 0.29' pd='2*int((1 + 1)/2) * (1.98 / 1 + 0.29)' ps='2*int((1 + 2)/2) * (1.98 / 1 + 0.29)'
+ nrd='0.29 / 1.98 ' nrs='0.29 / 1.98 ' sa=0 sb=0 sd=0 mult=1 m=1
XMmirrgB2 net4 BiasCB[2] net5 GndA sky130_fd_pr__nfet_01v8_lvt L=5 W=1.98 nf=1 ad='int((1 + 1)/2) * 1.98 / 1 * 0.29'
+ as='int((1 + 2)/2) * 1.98 / 1 * 0.29' pd='2*int((1 + 1)/2) * (1.98 / 1 + 0.29)' ps='2*int((1 + 2)/2) * (1.98 / 1 + 0.29)'
+ nrd='0.29 / 1.98 ' nrs='0.29 / 1.98 ' sa=0 sb=0 sd=0 mult=1 m=1
XMmirrfB2 net5 BiasCB[2] net6 GndA sky130_fd_pr__nfet_01v8_lvt L=5 W=1.98 nf=1 ad='int((1 + 1)/2) * 1.98 / 1 * 0.29'
+ as='int((1 + 2)/2) * 1.98 / 1 * 0.29' pd='2*int((1 + 1)/2) * (1.98 / 1 + 0.29)' ps='2*int((1 + 2)/2) * (1.98 / 1 + 0.29)'
+ nrd='0.29 / 1.98 ' nrs='0.29 / 1.98 ' sa=0 sb=0 sd=0 mult=1 m=1
XMmirrfB1 net6 BiasCB[2] net7 GndA sky130_fd_pr__nfet_01v8_lvt L=5 W=1.98 nf=1 ad='int((1 + 1)/2) * 1.98 / 1 * 0.29'
+ as='int((1 + 2)/2) * 1.98 / 1 * 0.29' pd='2*int((1 + 1)/2) * (1.98 / 1 + 0.29)' ps='2*int((1 + 2)/2) * (1.98 / 1 + 0.29)'
+ nrd='0.29 / 1.98 ' nrs='0.29 / 1.98 ' sa=0 sb=0 sd=0 mult=1 m=1
XMmirreB2 net7 BiasCB[2] net8 GndA sky130_fd_pr__nfet_01v8_lvt L=5 W=1.98 nf=1 ad='int((1 + 1)/2) * 1.98 / 1 * 0.29'
+ as='int((1 + 2)/2) * 1.98 / 1 * 0.29' pd='2*int((1 + 1)/2) * (1.98 / 1 + 0.29)' ps='2*int((1 + 2)/2) * (1.98 / 1 + 0.29)'
+ nrd='0.29 / 1.98 ' nrs='0.29 / 1.98 ' sa=0 sb=0 sd=0 mult=1 m=1
XMmirrcB2 net8 BiasCB[2] net9 GndA sky130_fd_pr__nfet_01v8_lvt L=5 W=1.98 nf=1 ad='int((1 + 1)/2) * 1.98 / 1 * 0.29'
+ as='int((1 + 2)/2) * 1.98 / 1 * 0.29' pd='2*int((1 + 1)/2) * (1.98 / 1 + 0.29)' ps='2*int((1 + 2)/2) * (1.98 / 1 + 0.29)'
+ nrd='0.29 / 1.98 ' nrs='0.29 / 1.98 ' sa=0 sb=0 sd=0 mult=1 m=1
XMmirrbB2 net9 BiasCB[2] net10 GndA sky130_fd_pr__nfet_01v8_lvt L=5 W=1.98 nf=1 ad='int((1 + 1)/2) * 1.98 / 1 * 0.29'
+ as='int((1 + 2)/2) * 1.98 / 1 * 0.29' pd='2*int((1 + 1)/2) * (1.98 / 1 + 0.29)' ps='2*int((1 + 2)/2) * (1.98 / 1 + 0.29)'
+ nrd='0.29 / 1.98 ' nrs='0.29 / 1.98 ' sa=0 sb=0 sd=0 mult=1 m=1
XMmirraB2 net10 BiasCB[2] GndA GndA sky130_fd_pr__nfet_01v8_lvt L=5 W=1.98 nf=1 ad='int((1 + 1)/2) * 1.98 / 1 * 0.29'
+ as='int((1 + 2)/2) * 1.98 / 1 * 0.29' pd='2*int((1 + 1)/2) * (1.98 / 1 + 0.29)' ps='2*int((1 + 2)/2) * (1.98 / 1 + 0.29)'
+ nrd='0.29 / 1.98 ' nrs='0.29 / 1.98 ' sa=0 sb=0 sd=0 mult=1 m=1
XMpswB3 net11 CoarseOneHot[3] VddA18 VddA18 sky130_fd_pr__pfet_01v8 L=0.15 W=0.55 nf=1 ad='int((1 + 1)/2) * 0.55 / 1 * 0.29'
+ as='int((1 + 2)/2) * 0.55 / 1 * 0.29' pd='2*int((1 + 1)/2) * (0.55 / 1 + 0.29)' ps='2*int((1 + 2)/2) * (0.55 / 1 + 0.29)'
+ nrd='0.29 / 0.55 ' nrs='0.29 / 0.55 ' sa=0 sb=0 sd=0 mult=1 m=1
XMnswuB3 CoarseBias CoarseOneHot[3] net11 GndA sky130_fd_pr__nfet_01v8 L=1 W=1 nf=1 ad='int((1 + 1)/2) * 1 / 1 * 0.29'
+ as='int((1 + 2)/2) * 1 / 1 * 0.29' pd='2*int((1 + 1)/2) * (1 / 1 + 0.29)' ps='2*int((1 + 2)/2) * (1 / 1 + 0.29)'
+ nrd='0.29 / 1 ' nrs='0.29 / 1 ' sa=0 sb=0 sd=0 mult=1 m=1
XMnswlB3 net11 CoarseOneHot[3] MirrB3_drain GndA sky130_fd_pr__nfet_01v8 L=1 W=1 nf=1 ad='int((1 + 1)/2) * 1 / 1 * 0.29'
+ as='int((1 + 2)/2) * 1 / 1 * 0.29' pd='2*int((1 + 1)/2) * (1 / 1 + 0.29)' ps='2*int((1 + 2)/2) * (1 / 1 + 0.29)'
+ nrd='0.29 / 1 ' nrs='0.29 / 1 ' sa=0 sb=0 sd=0 mult=1 m=1
XMmirrhB3 MirrB3_drain BiasCB[3] net12 GndA sky130_fd_pr__nfet_01v8_lvt L=9.98 W=0.98 nf=1 ad='int((1 + 1)/2) * 0.98 / 1 * 0.29'
+ as='int((1 + 2)/2) * 0.98 / 1 * 0.29' pd='2*int((1 + 1)/2) * (0.98 / 1 + 0.29)' ps='2*int((1 + 2)/2) * (0.98 / 1 + 0.29)'
+ nrd='0.29 / 0.98 ' nrs='0.29 / 0.98 ' sa=0 sb=0 sd=0 mult=1 m=1
XMmirrgB3 net12 BiasCB[3] net13 GndA sky130_fd_pr__nfet_01v8_lvt L=9.98 W=0.98 nf=1 ad='int((1 + 1)/2) * 0.98 / 1 * 0.29'
+ as='int((1 + 2)/2) * 0.98 / 1 * 0.29' pd='2*int((1 + 1)/2) * (0.98 / 1 + 0.29)' ps='2*int((1 + 2)/2) * (0.98 / 1 + 0.29)'
+ nrd='0.29 / 0.98 ' nrs='0.29 / 0.98 ' sa=0 sb=0 sd=0 mult=1 m=1
XMmirrfB3 net13 BiasCB[3] net14 GndA sky130_fd_pr__nfet_01v8_lvt L=9.98 W=0.98 nf=1 ad='int((1 + 1)/2) * 0.98 / 1 * 0.29'
+ as='int((1 + 2)/2) * 0.98 / 1 * 0.29' pd='2*int((1 + 1)/2) * (0.98 / 1 + 0.29)' ps='2*int((1 + 2)/2) * (0.98 / 1 + 0.29)'
+ nrd='0.29 / 0.98 ' nrs='0.29 / 0.98 ' sa=0 sb=0 sd=0 mult=1 m=1
XMmirreB3 net14 BiasCB[3] net15 GndA sky130_fd_pr__nfet_01v8_lvt L=9.98 W=0.98 nf=1 ad='int((1 + 1)/2) * 0.98 / 1 * 0.29'
+ as='int((1 + 2)/2) * 0.98 / 1 * 0.29' pd='2*int((1 + 1)/2) * (0.98 / 1 + 0.29)' ps='2*int((1 + 2)/2) * (0.98 / 1 + 0.29)'
+ nrd='0.29 / 0.98 ' nrs='0.29 / 0.98 ' sa=0 sb=0 sd=0 mult=1 m=1
XMmirrdB3 net15 BiasCB[3] net16 GndA sky130_fd_pr__nfet_01v8_lvt L=9.98 W=0.98 nf=1 ad='int((1 + 1)/2) * 0.98 / 1 * 0.29'
+ as='int((1 + 2)/2) * 0.98 / 1 * 0.29' pd='2*int((1 + 1)/2) * (0.98 / 1 + 0.29)' ps='2*int((1 + 2)/2) * (0.98 / 1 + 0.29)'
+ nrd='0.29 / 0.98 ' nrs='0.29 / 0.98 ' sa=0 sb=0 sd=0 mult=1 m=1
XMmirrcB3 net16 BiasCB[3] net17 GndA sky130_fd_pr__nfet_01v8_lvt L=9.98 W=0.98 nf=1 ad='int((1 + 1)/2) * 0.98 / 1 * 0.29'
+ as='int((1 + 2)/2) * 0.98 / 1 * 0.29' pd='2*int((1 + 1)/2) * (0.98 / 1 + 0.29)' ps='2*int((1 + 2)/2) * (0.98 / 1 + 0.29)'
+ nrd='0.29 / 0.98 ' nrs='0.29 / 0.98 ' sa=0 sb=0 sd=0 mult=1 m=1
XMmirrbB3 net17 BiasCB[3] net18 GndA sky130_fd_pr__nfet_01v8_lvt L=9.98 W=0.98 nf=1 ad='int((1 + 1)/2) * 0.98 / 1 * 0.29'
+ as='int((1 + 2)/2) * 0.98 / 1 * 0.29' pd='2*int((1 + 1)/2) * (0.98 / 1 + 0.29)' ps='2*int((1 + 2)/2) * (0.98 / 1 + 0.29)'
+ nrd='0.29 / 0.98 ' nrs='0.29 / 0.98 ' sa=0 sb=0 sd=0 mult=1 m=1
XMmirraB3 net18 BiasCB[3] GndA GndA sky130_fd_pr__nfet_01v8_lvt L=9.98 W=0.98 nf=1 ad='int((1 + 1)/2) * 0.98 / 1 * 0.29'
+ as='int((1 + 2)/2) * 0.98 / 1 * 0.29' pd='2*int((1 + 1)/2) * (0.98 / 1 + 0.29)' ps='2*int((1 + 2)/2) * (0.98 / 1 + 0.29)'
+ nrd='0.29 / 0.98 ' nrs='0.29 / 0.98 ' sa=0 sb=0 sd=0 mult=1 m=1
XMnswuB4to7 CoarseBias CoarseOneHotLowBiasEn MirrB4o5o6o7_drain GndA sky130_fd_pr__nfet_01v8 L=1 W=1
+ nf=1 ad='int((1 + 1)/2) * 1 / 1 * 0.29' as='int((1 + 2)/2) * 1 / 1 * 0.29' pd='2*int((1 + 1)/2) * (1 / 1 + 0.29)'
+ ps='2*int((1 + 2)/2) * (1 / 1 + 0.29)' nrd='0.29 / 1 ' nrs='0.29 / 1 ' sa=0 sb=0 sd=0 mult=1 m=1
XMmirrhB4to7 MirrB4o5o6o7_drain MirrB4o5o6o7_gate net19 GndA sky130_fd_pr__nfet_01v8_lvt L=20 W=0.5 nf=1
+ ad='int((1 + 1)/2) * 0.5 / 1 * 0.29' as='int((1 + 2)/2) * 0.5 / 1 * 0.29' pd='2*int((1 + 1)/2) * (0.5 / 1 + 0.29)'
+ ps='2*int((1 + 2)/2) * (0.5 / 1 + 0.29)' nrd='0.29 / 0.5 ' nrs='0.29 / 0.5 ' sa=0 sb=0 sd=0 mult=1 m=1
XMmirraB4to7 net25 MirrB4o5o6o7_gate GndA GndA sky130_fd_pr__nfet_01v8_lvt L=20 W=0.5 nf=1 ad='int((1 + 1)/2) * 0.5 / 1 * 0.29'
+ as='int((1 + 2)/2) * 0.5 / 1 * 0.29' pd='2*int((1 + 1)/2) * (0.5 / 1 + 0.29)' ps='2*int((1 + 2)/2) * (0.5 / 1 + 0.29)'
+ nrd='0.29 / 0.5 ' nrs='0.29 / 0.5 ' sa=0 sb=0 sd=0 mult=1 m=1
XMmirrbB4to7 net24 MirrB4o5o6o7_gate net25 GndA sky130_fd_pr__nfet_01v8_lvt L=20 W=0.5 nf=1 ad='int((1 + 1)/2) * 0.5 / 1 * 0.29'
+ as='int((1 + 2)/2) * 0.5 / 1 * 0.29' pd='2*int((1 + 1)/2) * (0.5 / 1 + 0.29)' ps='2*int((1 + 2)/2) * (0.5 / 1 + 0.29)'
+ nrd='0.29 / 0.5 ' nrs='0.29 / 0.5 ' sa=0 sb=0 sd=0 mult=1 m=1
XMmirrcB4to7 net23 MirrB4o5o6o7_gate net24 GndA sky130_fd_pr__nfet_01v8_lvt L=20 W=0.5 nf=1 ad='int((1 + 1)/2) * 0.5 / 1 * 0.29'
+ as='int((1 + 2)/2) * 0.5 / 1 * 0.29' pd='2*int((1 + 1)/2) * (0.5 / 1 + 0.29)' ps='2*int((1 + 2)/2) * (0.5 / 1 + 0.29)'
+ nrd='0.29 / 0.5 ' nrs='0.29 / 0.5 ' sa=0 sb=0 sd=0 mult=1 m=1
XMmirrdB4to7 net22 MirrB4o5o6o7_gate net23 GndA sky130_fd_pr__nfet_01v8_lvt L=20 W=0.5 nf=1 ad='int((1 + 1)/2) * 0.5 / 1 * 0.29'
+ as='int((1 + 2)/2) * 0.5 / 1 * 0.29' pd='2*int((1 + 1)/2) * (0.5 / 1 + 0.29)' ps='2*int((1 + 2)/2) * (0.5 / 1 + 0.29)'
+ nrd='0.29 / 0.5 ' nrs='0.29 / 0.5 ' sa=0 sb=0 sd=0 mult=1 m=1
XMmirreB4to7 net21 MirrB4o5o6o7_gate net22 GndA sky130_fd_pr__nfet_01v8_lvt L=20 W=0.5 nf=1 ad='int((1 + 1)/2) * 0.5 / 1 * 0.29'
+ as='int((1 + 2)/2) * 0.5 / 1 * 0.29' pd='2*int((1 + 1)/2) * (0.5 / 1 + 0.29)' ps='2*int((1 + 2)/2) * (0.5 / 1 + 0.29)'
+ nrd='0.29 / 0.5 ' nrs='0.29 / 0.5 ' sa=0 sb=0 sd=0 mult=1 m=1
XMmirrfB4to7 net20 MirrB4o5o6o7_gate net21 GndA sky130_fd_pr__nfet_01v8_lvt L=20 W=0.5 nf=1 ad='int((1 + 1)/2) * 0.5 / 1 * 0.29'
+ as='int((1 + 2)/2) * 0.5 / 1 * 0.29' pd='2*int((1 + 1)/2) * (0.5 / 1 + 0.29)' ps='2*int((1 + 2)/2) * (0.5 / 1 + 0.29)'
+ nrd='0.29 / 0.5 ' nrs='0.29 / 0.5 ' sa=0 sb=0 sd=0 mult=1 m=1
XMmirrgB4to7 net19 MirrB4o5o6o7_gate net20 GndA sky130_fd_pr__nfet_01v8_lvt L=20 W=0.5 nf=1 ad='int((1 + 1)/2) * 0.5 / 1 * 0.29'
+ as='int((1 + 2)/2) * 0.5 / 1 * 0.29' pd='2*int((1 + 1)/2) * (0.5 / 1 + 0.29)' ps='2*int((1 + 2)/2) * (0.5 / 1 + 0.29)'
+ nrd='0.29 / 0.5 ' nrs='0.29 / 0.5 ' sa=0 sb=0 sd=0 mult=1 m=1
XMnswl7 MirrB4o5o6o7_gate CoarseOneHot[7] BiasCB[7] GndA sky130_fd_pr__nfet_01v8 L=1 W=1 nf=1 ad='int((1 + 1)/2) * 1 / 1 * 0.29'
+ as='int((1 + 2)/2) * 1 / 1 * 0.29' pd='2*int((1 + 1)/2) * (1 / 1 + 0.29)' ps='2*int((1 + 2)/2) * (1 / 1 + 0.29)'
+ nrd='0.29 / 1 ' nrs='0.29 / 1 ' sa=0 sb=0 sd=0 mult=1 m=1
XMnswlB6 MirrB4o5o6o7_gate CoarseOneHot[6] BiasCB[6] GndA sky130_fd_pr__nfet_01v8 L=1 W=1 nf=1 ad='int((1 + 1)/2) * 1 / 1 * 0.29'
+ as='int((1 + 2)/2) * 1 / 1 * 0.29' pd='2*int((1 + 1)/2) * (1 / 1 + 0.29)' ps='2*int((1 + 2)/2) * (1 / 1 + 0.29)'
+ nrd='0.29 / 1 ' nrs='0.29 / 1 ' sa=0 sb=0 sd=0 mult=1 m=1
XMnswlB5 MirrB4o5o6o7_gate CoarseOneHot[5] BiasCB[5] GndA sky130_fd_pr__nfet_01v8 L=1 W=1 nf=1 ad='int((1 + 1)/2) * 1 / 1 * 0.29'
+ as='int((1 + 2)/2) * 1 / 1 * 0.29' pd='2*int((1 + 1)/2) * (1 / 1 + 0.29)' ps='2*int((1 + 2)/2) * (1 / 1 + 0.29)'
+ nrd='0.29 / 1 ' nrs='0.29 / 1 ' sa=0 sb=0 sd=0 mult=1 m=1
XMnswlB4 MirrB4o5o6o7_gate CoarseOneHot[4] BiasCB[4] GndA sky130_fd_pr__nfet_01v8 L=1 W=1 nf=1 ad='int((1 + 1)/2) * 1 / 1 * 0.29'
+ as='int((1 + 2)/2) * 1 / 1 * 0.29' pd='2*int((1 + 1)/2) * (1 / 1 + 0.29)' ps='2*int((1 + 2)/2) * (1 / 1 + 0.29)'
+ nrd='0.29 / 1 ' nrs='0.29 / 1 ' sa=0 sb=0 sd=0 mult=1 m=1
.ends


* expanding   symbol:  BiasDividerFineCell.sym # of pins=8
** sym_path: analog/xschem/BiasDividerFineCell.sym
** sch_path: analog/xschem/BiasDividerFineCell.sch
.subckt BiasDividerFineCell IPrev INext VGate IOut VddA18 INOut nSel Sel
*.iopin INext
*.iopin IOut
*.iopin IPrev
*.ipin VGate
*.iopin VddA18
*.ipin nSel
*.ipin Sel
*.iopin INOut
XMr INext VGate IPrev VddA18 sky130_fd_pr__pfet_01v8 L=1 W=9 nf=1 ad='int((1 + 1)/2) * 9 / 1 * 0.29'
+ as='int((1 + 2)/2) * 9 / 1 * 0.29' pd='2*int((1 + 1)/2) * (9 / 1 + 0.29)' ps='2*int((1 + 2)/2) * (9 / 1 + 0.29)'
+ nrd='0.29 / 9 ' nrs='0.29 / 9 ' sa=0 sb=0 sd=0 mult=2 m=2
XM2ru net1 VGate IPrev VddA18 sky130_fd_pr__pfet_01v8 L=1 W=9 nf=1 ad='int((1 + 1)/2) * 9 / 1 * 0.29'
+ as='int((1 + 2)/2) * 9 / 1 * 0.29' pd='2*int((1 + 1)/2) * (9 / 1 + 0.29)' ps='2*int((1 + 2)/2) * (9 / 1 + 0.29)'
+ nrd='0.29 / 9 ' nrs='0.29 / 9 ' sa=0 sb=0 sd=0 mult=2 m=2
XM2rl net2 VGate net1 VddA18 sky130_fd_pr__pfet_01v8 L=1 W=9 nf=1 ad='int((1 + 1)/2) * 9 / 1 * 0.29'
+ as='int((1 + 2)/2) * 9 / 1 * 0.29' pd='2*int((1 + 1)/2) * (9 / 1 + 0.29)' ps='2*int((1 + 2)/2) * (9 / 1 + 0.29)'
+ nrd='0.29 / 9 ' nrs='0.29 / 9 ' sa=0 sb=0 sd=0 mult=2 m=2
XMswNOut INOut Sel net2 VddA18 sky130_fd_pr__pfet_01v8 L=0.5 W=2 nf=1 ad='int((1 + 1)/2) * 2 / 1 * 0.29'
+ as='int((1 + 2)/2) * 2 / 1 * 0.29' pd='2*int((1 + 1)/2) * (2 / 1 + 0.29)' ps='2*int((1 + 2)/2) * (2 / 1 + 0.29)'
+ nrd='0.29 / 2 ' nrs='0.29 / 2 ' sa=0 sb=0 sd=0 mult=1 m=1
XMswOut IOut nSel net2 VddA18 sky130_fd_pr__pfet_01v8 L=0.5 W=2 nf=1 ad='int((1 + 1)/2) * 2 / 1 * 0.29'
+ as='int((1 + 2)/2) * 2 / 1 * 0.29' pd='2*int((1 + 1)/2) * (2 / 1 + 0.29)' ps='2*int((1 + 2)/2) * (2 / 1 + 0.29)'
+ nrd='0.29 / 2 ' nrs='0.29 / 2 ' sa=0 sb=0 sd=0 mult=1 m=1
.ends

.end
